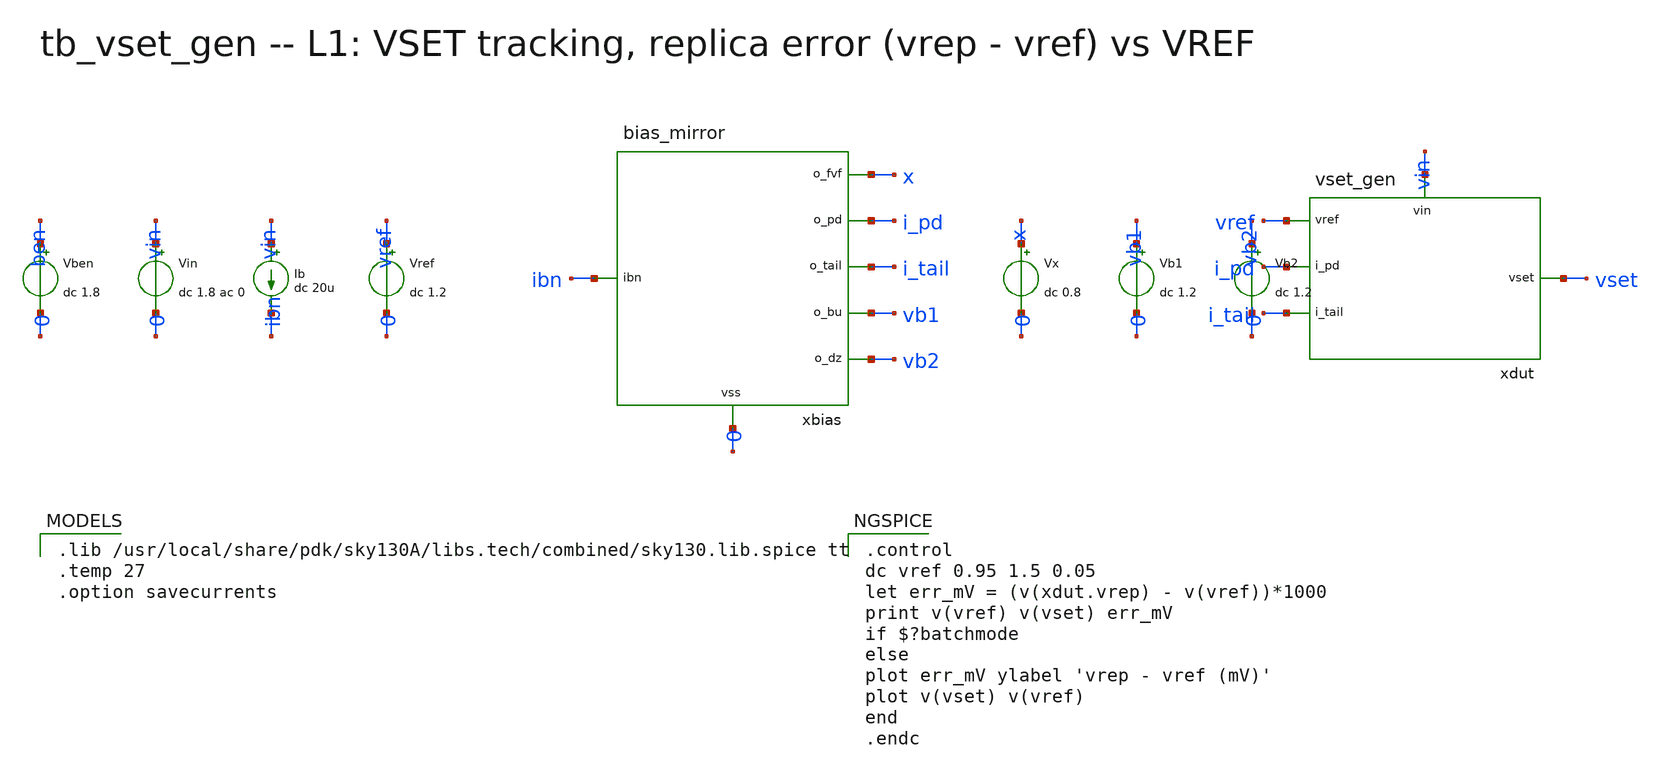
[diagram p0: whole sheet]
** sch_path: xschem/onetops_tb/tb_vset_gen.sch
**.subckt tb_vset_gen
Vin vin 0 dc 1.8 ac 0
Ib vin ibn dc 20u
Vben ben 0 dc 1.8
Vref vref 0 dc 1.2
xbias ibn x i_pd i_tail vb1 vb2 0 bias_mirror
Vx x 0 dc 0.8
Vb1 vb1 0 dc 1.2
Vb2 vb2 0 dc 1.2
xdut vref i_pd i_tail vset vin vset_gen
**** begin user architecture code

.lib /usr/local/share/pdk/sky130A/libs.tech/combined/sky130.lib.spice tt
.temp 27
.option savecurrents


.control
dc vref 0.95 1.5 0.05
let err_mV = (v(xdut.vrep) - v(vref))*1000
print v(vref) v(vset) err_mV
if $?batchmode
else
plot err_mV ylabel 'vrep - vref (mV)'
plot v(vset) v(vref)
end
.endc

**** end user architecture code
**.ends

* expanding   symbol:  onetops/bias_mirror.sym # of pins=7
** sym_path: xschem/onetops/bias_mirror.sym
** sch_path: xschem/onetops/bias_mirror.sch
.subckt bias_mirror ibn o_fvf o_pd o_tail o_bu o_dz vss
*.ipin ibn
*.opin o_fvf
*.opin o_pd
*.opin o_tail
*.opin o_bu
*.opin o_dz
*.iopin vss
XMN0 ibn ibn vss vss sky130_fd_pr__nfet_01v8 L=1 W=4 nf=1 ad='int((1 + 1)/2) * 4 / 1 * 0.29' as='int((1 + 2)/2) * 4 / 1 * 0.29'
+ pd='2*int((1 + 1)/2) * (4 / 1 + 0.29)' ps='2*int((1 + 2)/2) * (4 / 1 + 0.29)' nrd='0.29 / 4 ' nrs='0.29 / 4 '
+ sa=0 sb=0 sd=0 mult=1 m=1
XMN1 o_fvf ibn vss vss sky130_fd_pr__nfet_01v8 L=1 W=4 nf=1 ad='int((1 + 1)/2) * 4 / 1 * 0.29' as='int((1 + 2)/2) * 4 / 1 * 0.29'
+ pd='2*int((1 + 1)/2) * (4 / 1 + 0.29)' ps='2*int((1 + 2)/2) * (4 / 1 + 0.29)' nrd='0.29 / 4 ' nrs='0.29 / 4 '
+ sa=0 sb=0 sd=0 mult=1 m=1
XMN2 o_bu ibn vss vss sky130_fd_pr__nfet_01v8 L=1 W=4 nf=1 ad='int((1 + 1)/2) * 4 / 1 * 0.29' as='int((1 + 2)/2) * 4 / 1 * 0.29'
+ pd='2*int((1 + 1)/2) * (4 / 1 + 0.29)' ps='2*int((1 + 2)/2) * (4 / 1 + 0.29)' nrd='0.29 / 4 ' nrs='0.29 / 4 '
+ sa=0 sb=0 sd=0 mult=1 m=1
XMN3 o_pd ibn vss vss sky130_fd_pr__nfet_01v8 L=1 W=4 nf=1 ad='int((1 + 1)/2) * 4 / 1 * 0.29' as='int((1 + 2)/2) * 4 / 1 * 0.29'
+ pd='2*int((1 + 1)/2) * (4 / 1 + 0.29)' ps='2*int((1 + 2)/2) * (4 / 1 + 0.29)' nrd='0.29 / 4 ' nrs='0.29 / 4 '
+ sa=0 sb=0 sd=0 mult=1 m=1
XMN4 o_tail ibn vss vss sky130_fd_pr__nfet_01v8 L=1 W=4 nf=1 ad='int((1 + 1)/2) * 4 / 1 * 0.29' as='int((1 + 2)/2) * 4 / 1 * 0.29'
+ pd='2*int((1 + 1)/2) * (4 / 1 + 0.29)' ps='2*int((1 + 2)/2) * (4 / 1 + 0.29)' nrd='0.29 / 4 ' nrs='0.29 / 4 '
+ sa=0 sb=0 sd=0 mult=2 m=2
XMN5 o_dz ibn vss vss sky130_fd_pr__nfet_01v8 L=1 W=4 nf=1 ad='int((1 + 1)/2) * 4 / 1 * 0.29' as='int((1 + 2)/2) * 4 / 1 * 0.29'
+ pd='2*int((1 + 1)/2) * (4 / 1 + 0.29)' ps='2*int((1 + 2)/2) * (4 / 1 + 0.29)' nrd='0.29 / 4 ' nrs='0.29 / 4 '
+ sa=0 sb=0 sd=0 mult=1 m=1
.ends


* expanding   symbol:  onetops/vset_gen.sym # of pins=5
** sym_path: xschem/onetops/vset_gen.sym
** sch_path: xschem/onetops/vset_gen.sch
.subckt vset_gen vref i_pd i_tail vset vin
*.ipin vref
*.opin vset
*.iopin i_pd
*.iopin i_tail
*.iopin vin
XMPD i_pd i_pd vin vin sky130_fd_pr__pfet_01v8_lvt L=2 W=10 nf=1 ad='int((1 + 1)/2) * 10 / 1 * 0.29'
+ as='int((1 + 2)/2) * 10 / 1 * 0.29' pd='2*int((1 + 1)/2) * (10 / 1 + 0.29)' ps='2*int((1 + 2)/2) * (10 / 1 + 0.29)'
+ nrd='0.29 / 10 ' nrs='0.29 / 10 ' sa=0 sb=0 sd=0 mult=1 m=1
XMPS vrep i_pd vin vin sky130_fd_pr__pfet_01v8_lvt L=2 W=10 nf=1 ad='int((1 + 1)/2) * 10 / 1 * 0.29'
+ as='int((1 + 2)/2) * 10 / 1 * 0.29' pd='2*int((1 + 1)/2) * (10 / 1 + 0.29)' ps='2*int((1 + 2)/2) * (10 / 1 + 0.29)'
+ nrd='0.29 / 10 ' nrs='0.29 / 10 ' sa=0 sb=0 sd=0 mult=1 m=1
XMR 0 vset vrep vrep sky130_fd_pr__pfet_01v8_lvt L=1 W=100 nf=1 ad='int((1 + 1)/2) * 100 / 1 * 0.29'
+ as='int((1 + 2)/2) * 100 / 1 * 0.29' pd='2*int((1 + 1)/2) * (100 / 1 + 0.29)' ps='2*int((1 + 2)/2) * (100 / 1 + 0.29)'
+ nrd='0.29 / 100 ' nrs='0.29 / 100 ' sa=0 sb=0 sd=0 mult=1 m=1
xota vref vrep i_tail vset vin ota5t
Cset vset 0 2p m=1
.ends


* expanding   symbol:  onetops/ota5t.sym # of pins=5
** sym_path: xschem/onetops/ota5t.sym
** sch_path: xschem/onetops/ota5t.sch
.subckt ota5t inp inn tail out vdd
*.ipin inp
*.ipin inn
*.opin out
*.iopin tail
*.iopin vdd
XMP1 nd nd vdd vdd sky130_fd_pr__pfet_01v8_lvt L=2 W=20 nf=1 ad='int((1 + 1)/2) * 20 / 1 * 0.29' as='int((1 + 2)/2) * 20 / 1 * 0.29'
+ pd='2*int((1 + 1)/2) * (20 / 1 + 0.29)' ps='2*int((1 + 2)/2) * (20 / 1 + 0.29)' nrd='0.29 / 20 ' nrs='0.29 / 20 '
+ sa=0 sb=0 sd=0 mult=1 m=1
XMP2 out nd vdd vdd sky130_fd_pr__pfet_01v8_lvt L=2 W=20 nf=1 ad='int((1 + 1)/2) * 20 / 1 * 0.29' as='int((1 + 2)/2) * 20 / 1 * 0.29'
+ pd='2*int((1 + 1)/2) * (20 / 1 + 0.29)' ps='2*int((1 + 2)/2) * (20 / 1 + 0.29)' nrd='0.29 / 20 ' nrs='0.29 / 20 '
+ sa=0 sb=0 sd=0 mult=1 m=1
XMN1 nd inp tail 0 sky130_fd_pr__nfet_01v8 L=1 W=5 nf=1 ad='int((1 + 1)/2) * 5 / 1 * 0.29' as='int((1 + 2)/2) * 5 / 1 * 0.29'
+ pd='2*int((1 + 1)/2) * (5 / 1 + 0.29)' ps='2*int((1 + 2)/2) * (5 / 1 + 0.29)' nrd='0.29 / 5 ' nrs='0.29 / 5 '
+ sa=0 sb=0 sd=0 mult=1 m=1
XMN2 out inn tail 0 sky130_fd_pr__nfet_01v8 L=1 W=5 nf=1 ad='int((1 + 1)/2) * 5 / 1 * 0.29' as='int((1 + 2)/2) * 5 / 1 * 0.29'
+ pd='2*int((1 + 1)/2) * (5 / 1 + 0.29)' ps='2*int((1 + 2)/2) * (5 / 1 + 0.29)' nrd='0.29 / 5 ' nrs='0.29 / 5 '
+ sa=0 sb=0 sd=0 mult=1 m=1
.ends

.end
